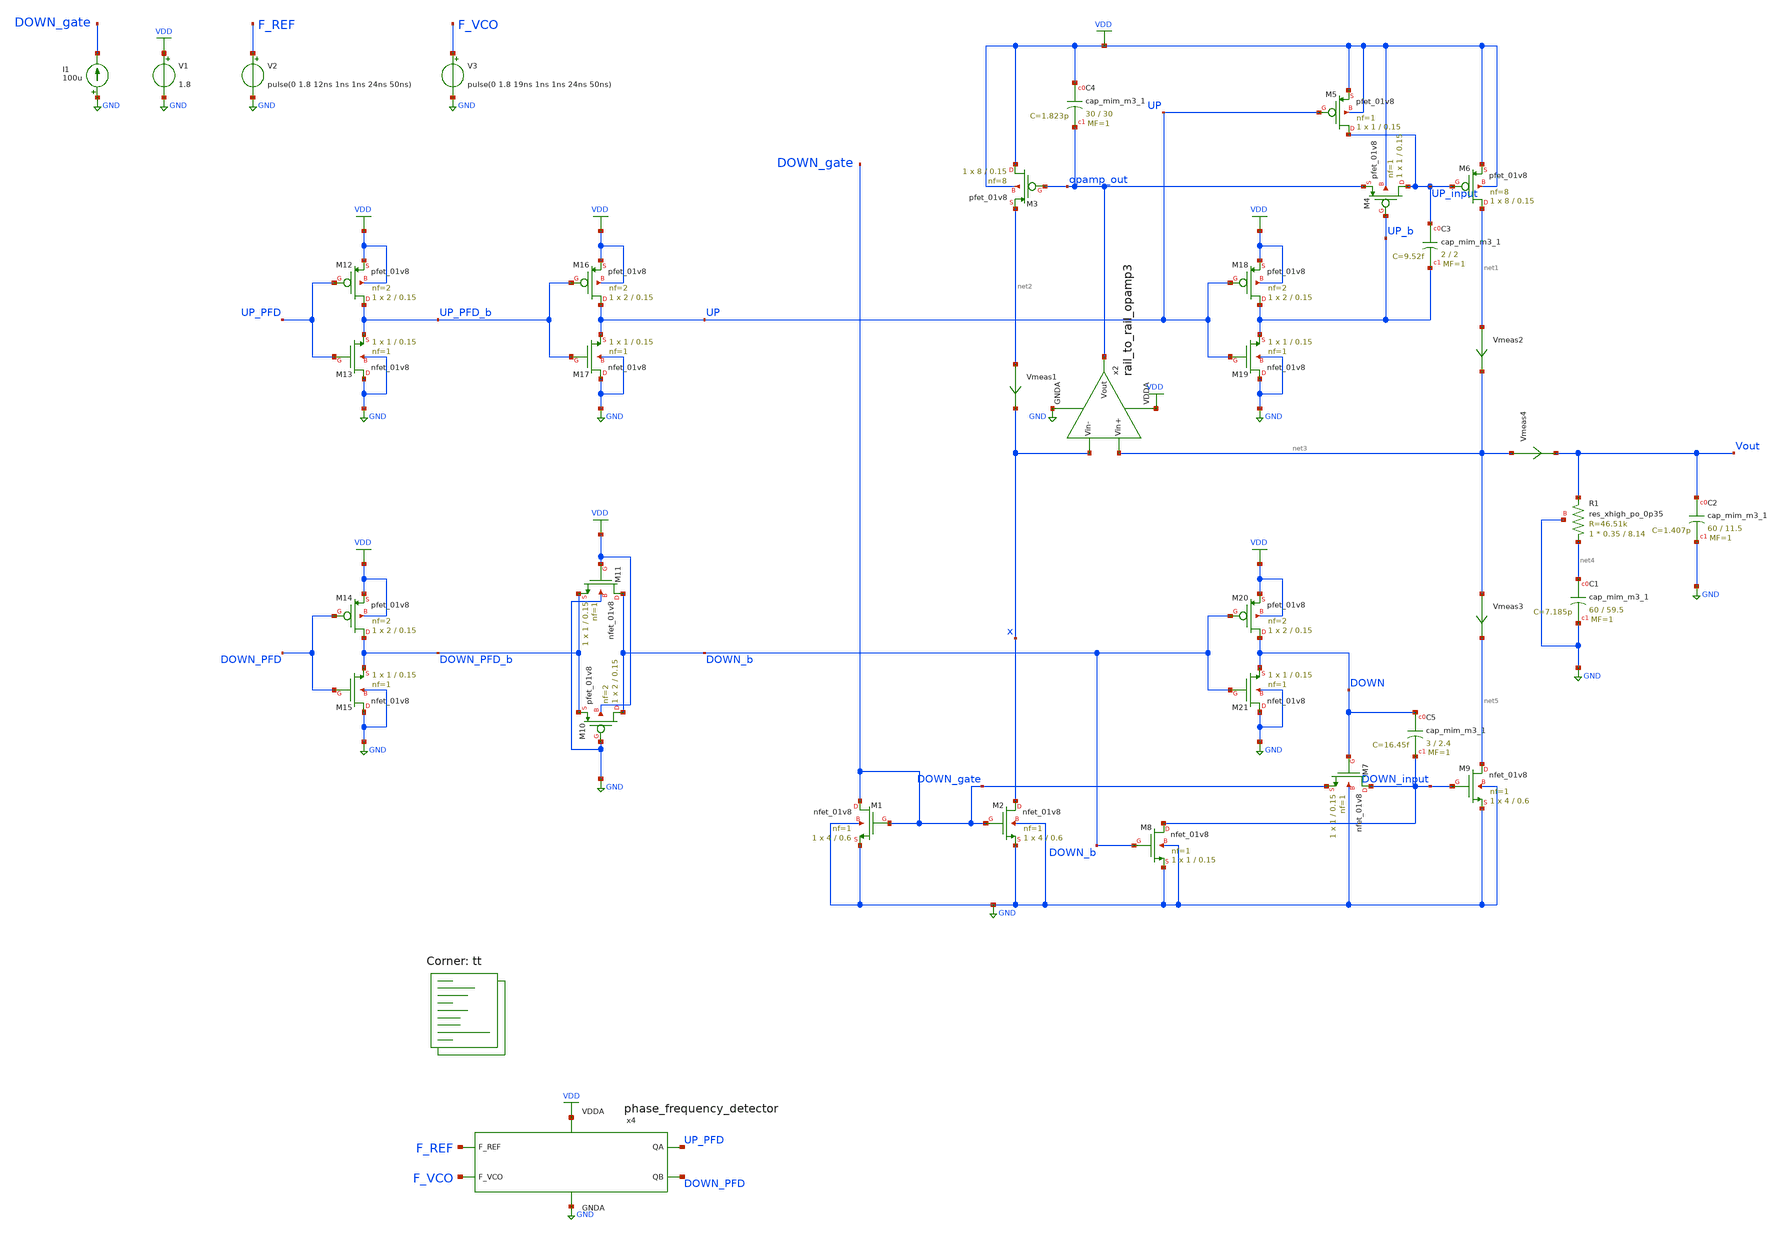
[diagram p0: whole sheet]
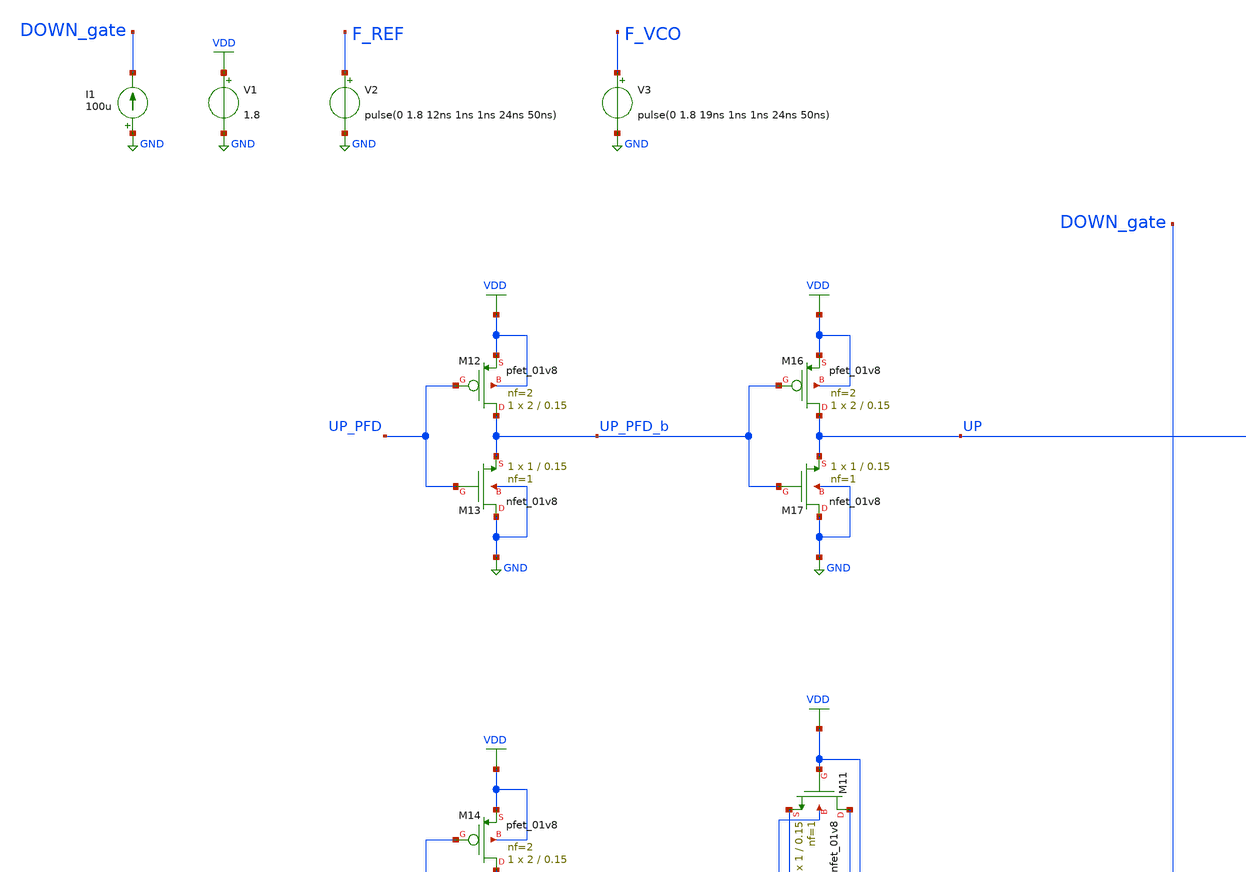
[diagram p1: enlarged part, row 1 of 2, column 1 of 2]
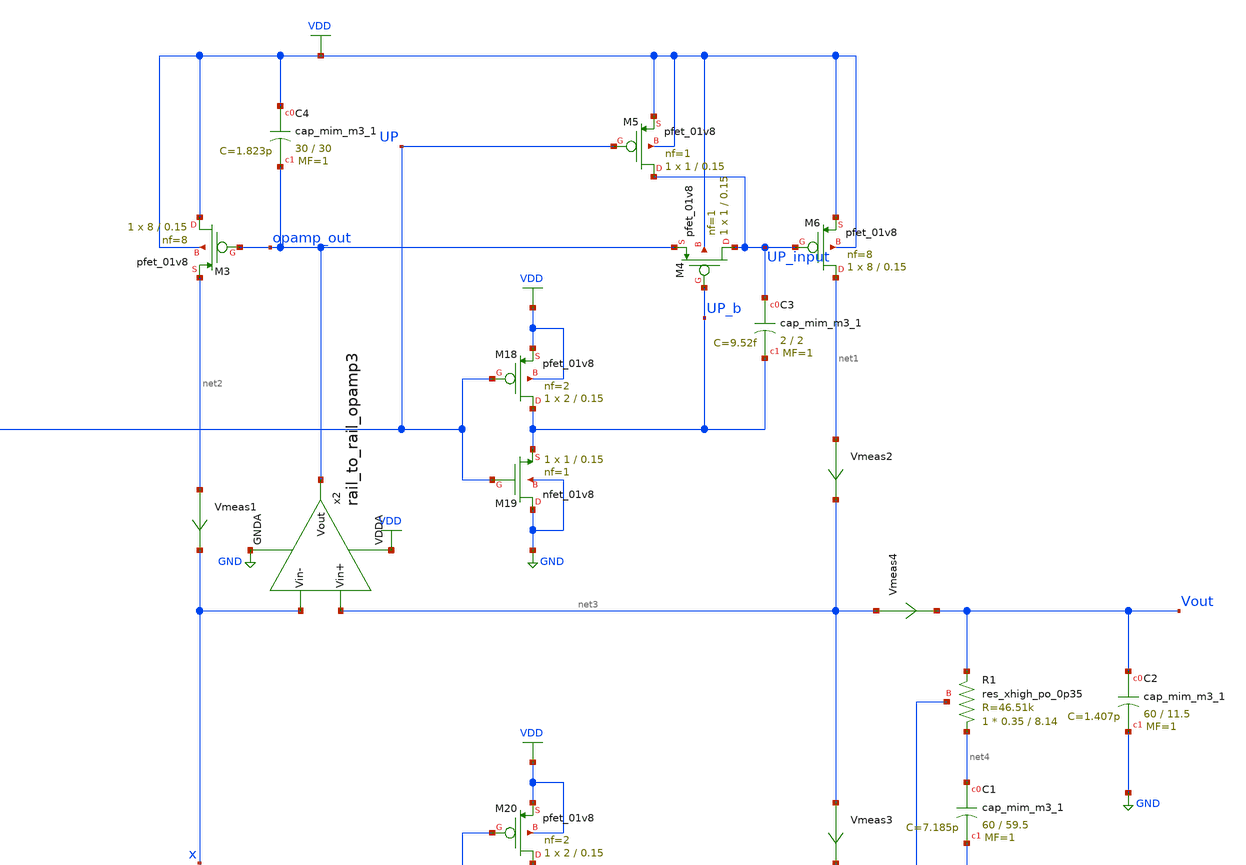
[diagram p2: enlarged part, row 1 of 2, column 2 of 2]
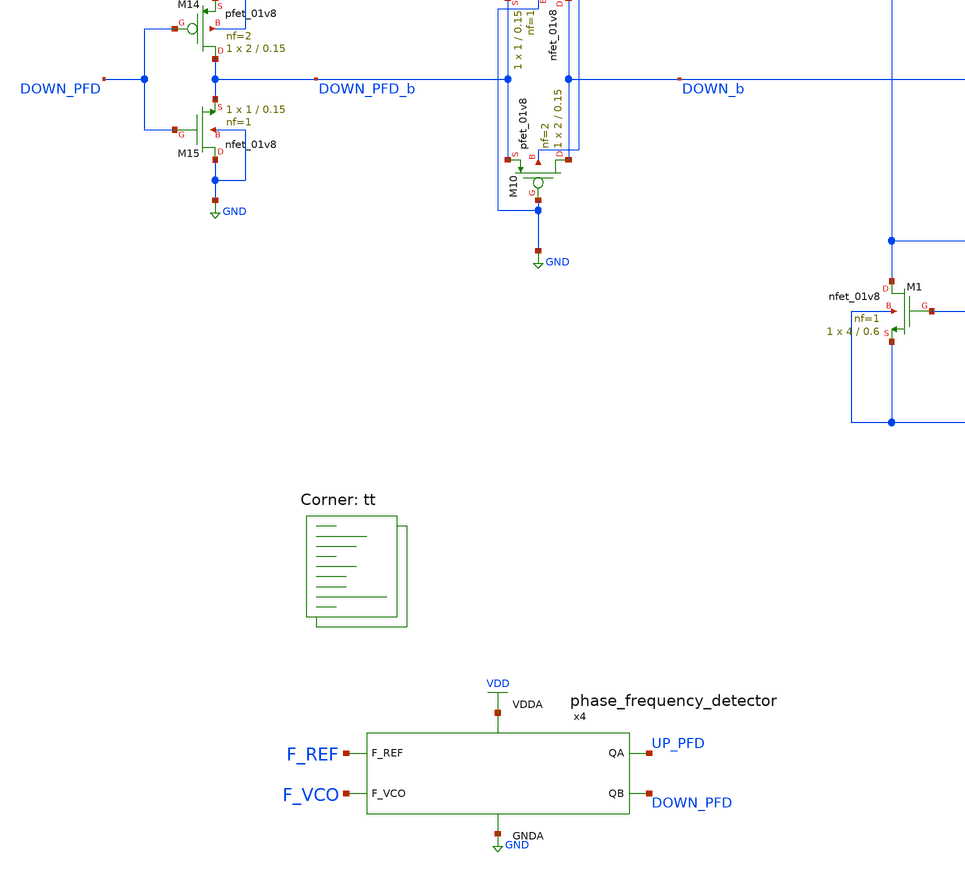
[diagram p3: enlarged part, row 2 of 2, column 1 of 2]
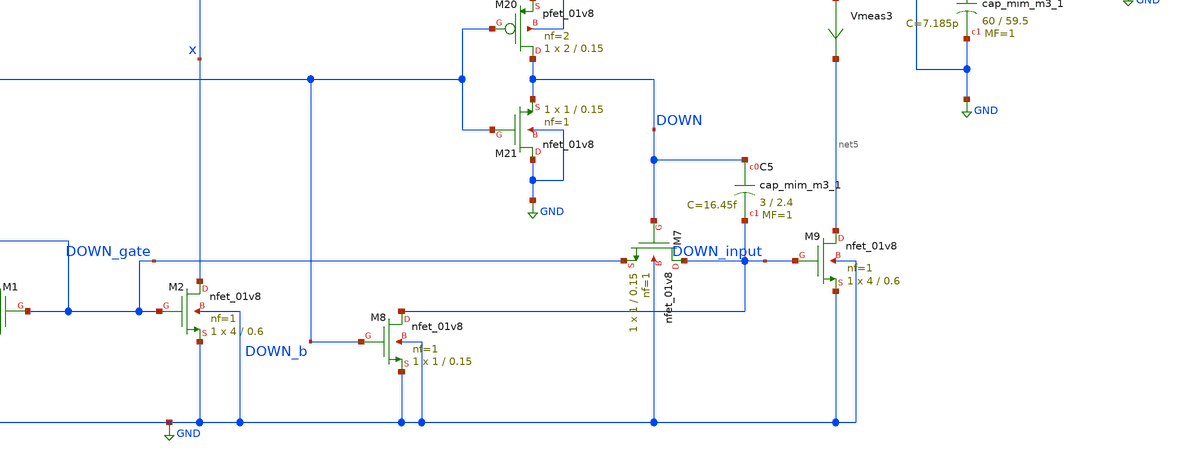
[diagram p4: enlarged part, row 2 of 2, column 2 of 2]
** sch_path: projects/pll/charge_pump/xschem_ngspice/pfd_charge_pump_7_2.sch
**.subckt pfd_charge_pump_7_2
V1 VDD GND 1.8
V2 F_REF GND pulse(0 1.8 12ns 1ns 1ns 24ns 50ns)
V3 F_VCO GND pulse(0 1.8 19ns 1ns 1ns 24ns 50ns)
x4 F_REF F_VCO VDD UP_PFD DOWN_PFD GND phase_frequency_detector
I1 GND DOWN_gate 100u
XM1 DOWN_gate DOWN_gate GND GND sky130_fd_pr__nfet_01v8 L=0.6 W=4 nf=1 ad='int((nf+1)/2) * W/nf * 0.29'
+ as='int((nf+2)/2) * W/nf * 0.29' pd='2*int((nf+1)/2) * (W/nf + 0.29)' ps='2*int((nf+2)/2) * (W/nf + 0.29)'
+ nrd='0.29 / W' nrs='0.29 / W' sa=0 sb=0 sd=0 mult=1 m=1
XM2 x DOWN_gate GND GND sky130_fd_pr__nfet_01v8 L=0.6 W=4 nf=1 ad='int((nf+1)/2) * W/nf * 0.29' as='int((nf+2)/2) * W/nf * 0.29'
+ pd='2*int((nf+1)/2) * (W/nf + 0.29)' ps='2*int((nf+2)/2) * (W/nf + 0.29)' nrd='0.29 / W' nrs='0.29 / W'
+ sa=0 sb=0 sd=0 mult=1 m=1
XM3 VDD opamp_out net2 VDD sky130_fd_pr__pfet_01v8 L=0.15 W=8 nf=8 ad='int((nf+1)/2) * W/nf * 0.29' as='int((nf+2)/2) * W/nf * 0.29'
+ pd='2*int((nf+1)/2) * (W/nf + 0.29)' ps='2*int((nf+2)/2) * (W/nf + 0.29)' nrd='0.29 / W' nrs='0.29 / W'
+ sa=0 sb=0 sd=0 mult=1 m=1
Vmeas1 net2 x 0
.save i(vmeas1)
XM4 UP_input UP_b opamp_out VDD sky130_fd_pr__pfet_01v8 L=0.15 W=1 nf=1 ad='int((nf+1)/2) * W/nf * 0.29'
+ as='int((nf+2)/2) * W/nf * 0.29' pd='2*int((nf+1)/2) * (W/nf + 0.29)' ps='2*int((nf+2)/2) * (W/nf + 0.29)'
+ nrd='0.29 / W' nrs='0.29 / W' sa=0 sb=0 sd=0 mult=1 m=1
XM5 UP_input UP VDD VDD sky130_fd_pr__pfet_01v8 L=0.15 W=1 nf=1 ad='int((nf+1)/2) * W/nf * 0.29' as='int((nf+2)/2) * W/nf * 0.29'
+ pd='2*int((nf+1)/2) * (W/nf + 0.29)' ps='2*int((nf+2)/2) * (W/nf + 0.29)' nrd='0.29 / W' nrs='0.29 / W'
+ sa=0 sb=0 sd=0 mult=1 m=1
XM6 net1 UP_input VDD VDD sky130_fd_pr__pfet_01v8 L=0.15 W=8 nf=8 ad='int((nf+1)/2) * W/nf * 0.29' as='int((nf+2)/2) * W/nf * 0.29'
+ pd='2*int((nf+1)/2) * (W/nf + 0.29)' ps='2*int((nf+2)/2) * (W/nf + 0.29)' nrd='0.29 / W' nrs='0.29 / W'
+ sa=0 sb=0 sd=0 mult=1 m=1
Vmeas2 net1 net3 0
.save i(vmeas2)
XM7 DOWN_input DOWN DOWN_gate GND sky130_fd_pr__nfet_01v8 L=0.15 W=1 nf=1 ad='int((nf+1)/2) * W/nf * 0.29'
+ as='int((nf+2)/2) * W/nf * 0.29' pd='2*int((nf+1)/2) * (W/nf + 0.29)' ps='2*int((nf+2)/2) * (W/nf + 0.29)'
+ nrd='0.29 / W' nrs='0.29 / W' sa=0 sb=0 sd=0 mult=1 m=1
XM8 DOWN_input DOWN_b GND GND sky130_fd_pr__nfet_01v8 L=0.15 W=1 nf=1 ad='int((nf+1)/2) * W/nf * 0.29'
+ as='int((nf+2)/2) * W/nf * 0.29' pd='2*int((nf+1)/2) * (W/nf + 0.29)' ps='2*int((nf+2)/2) * (W/nf + 0.29)'
+ nrd='0.29 / W' nrs='0.29 / W' sa=0 sb=0 sd=0 mult=1 m=1
Vmeas3 net3 net5 0
.save i(vmeas3)
XM9 net5 DOWN_input GND GND sky130_fd_pr__nfet_01v8 L=0.6 W=4 nf=1 ad='int((nf+1)/2) * W/nf * 0.29' as='int((nf+2)/2) * W/nf * 0.29'
+ pd='2*int((nf+1)/2) * (W/nf + 0.29)' ps='2*int((nf+2)/2) * (W/nf + 0.29)' nrd='0.29 / W' nrs='0.29 / W'
+ sa=0 sb=0 sd=0 mult=1 m=1
XC2 Vout GND sky130_fd_pr__cap_mim_m3_1 W=60 L=11.5 MF=1 m=1
XC1 net4 GND sky130_fd_pr__cap_mim_m3_1 W=60 L=59.5 MF=1 m=1
Vmeas4 net3 Vout 0
.save i(vmeas4)
x2 VDD net3 x opamp_out GND rail_to_rail_opamp3
XC4 VDD opamp_out sky130_fd_pr__cap_mim_m3_1 W=30 L=30 MF=1 m=1
XC3 UP_input UP_b sky130_fd_pr__cap_mim_m3_1 W=2 L=2 MF=1 m=1
XC5 DOWN DOWN_input sky130_fd_pr__cap_mim_m3_1 W=3 L=2.4 MF=1 m=1
XM10 DOWN_b GND DOWN_PFD_b VDD sky130_fd_pr__pfet_01v8 L=0.15 W=2 nf=2 ad='int((nf+1)/2) * W/nf * 0.29'
+ as='int((nf+2)/2) * W/nf * 0.29' pd='2*int((nf+1)/2) * (W/nf + 0.29)' ps='2*int((nf+2)/2) * (W/nf + 0.29)'
+ nrd='0.29 / W' nrs='0.29 / W' sa=0 sb=0 sd=0 mult=1 m=1
XM11 DOWN_b VDD DOWN_PFD_b GND sky130_fd_pr__nfet_01v8 L=0.15 W=1 nf=1 ad='int((nf+1)/2) * W/nf * 0.29'
+ as='int((nf+2)/2) * W/nf * 0.29' pd='2*int((nf+1)/2) * (W/nf + 0.29)' ps='2*int((nf+2)/2) * (W/nf + 0.29)'
+ nrd='0.29 / W' nrs='0.29 / W' sa=0 sb=0 sd=0 mult=1 m=1
XM12 UP_PFD_b UP_PFD VDD VDD sky130_fd_pr__pfet_01v8 L=0.15 W=2 nf=2 ad='int((nf+1)/2) * W/nf * 0.29'
+ as='int((nf+2)/2) * W/nf * 0.29' pd='2*int((nf+1)/2) * (W/nf + 0.29)' ps='2*int((nf+2)/2) * (W/nf + 0.29)'
+ nrd='0.29 / W' nrs='0.29 / W' sa=0 sb=0 sd=0 mult=1 m=1
XM13 GND UP_PFD UP_PFD_b GND sky130_fd_pr__nfet_01v8 L=0.15 W=1 nf=1 ad='int((nf+1)/2) * W/nf * 0.29'
+ as='int((nf+2)/2) * W/nf * 0.29' pd='2*int((nf+1)/2) * (W/nf + 0.29)' ps='2*int((nf+2)/2) * (W/nf + 0.29)'
+ nrd='0.29 / W' nrs='0.29 / W' sa=0 sb=0 sd=0 mult=1 m=1
XM14 DOWN_PFD_b DOWN_PFD VDD VDD sky130_fd_pr__pfet_01v8 L=0.15 W=2 nf=2 ad='int((nf+1)/2) * W/nf * 0.29'
+ as='int((nf+2)/2) * W/nf * 0.29' pd='2*int((nf+1)/2) * (W/nf + 0.29)' ps='2*int((nf+2)/2) * (W/nf + 0.29)'
+ nrd='0.29 / W' nrs='0.29 / W' sa=0 sb=0 sd=0 mult=1 m=1
XM15 GND DOWN_PFD DOWN_PFD_b GND sky130_fd_pr__nfet_01v8 L=0.15 W=1 nf=1 ad='int((nf+1)/2) * W/nf * 0.29'
+ as='int((nf+2)/2) * W/nf * 0.29' pd='2*int((nf+1)/2) * (W/nf + 0.29)' ps='2*int((nf+2)/2) * (W/nf + 0.29)'
+ nrd='0.29 / W' nrs='0.29 / W' sa=0 sb=0 sd=0 mult=1 m=1
XM16 UP UP_PFD_b VDD VDD sky130_fd_pr__pfet_01v8 L=0.15 W=2 nf=2 ad='int((nf+1)/2) * W/nf * 0.29' as='int((nf+2)/2) * W/nf * 0.29'
+ pd='2*int((nf+1)/2) * (W/nf + 0.29)' ps='2*int((nf+2)/2) * (W/nf + 0.29)' nrd='0.29 / W' nrs='0.29 / W'
+ sa=0 sb=0 sd=0 mult=1 m=1
XM17 GND UP_PFD_b UP GND sky130_fd_pr__nfet_01v8 L=0.15 W=1 nf=1 ad='int((nf+1)/2) * W/nf * 0.29' as='int((nf+2)/2) * W/nf * 0.29'
+ pd='2*int((nf+1)/2) * (W/nf + 0.29)' ps='2*int((nf+2)/2) * (W/nf + 0.29)' nrd='0.29 / W' nrs='0.29 / W'
+ sa=0 sb=0 sd=0 mult=1 m=1
XM18 UP_b UP VDD VDD sky130_fd_pr__pfet_01v8 L=0.15 W=2 nf=2 ad='int((nf+1)/2) * W/nf * 0.29' as='int((nf+2)/2) * W/nf * 0.29'
+ pd='2*int((nf+1)/2) * (W/nf + 0.29)' ps='2*int((nf+2)/2) * (W/nf + 0.29)' nrd='0.29 / W' nrs='0.29 / W'
+ sa=0 sb=0 sd=0 mult=1 m=1
XM19 GND UP UP_b GND sky130_fd_pr__nfet_01v8 L=0.15 W=1 nf=1 ad='int((nf+1)/2) * W/nf * 0.29' as='int((nf+2)/2) * W/nf * 0.29'
+ pd='2*int((nf+1)/2) * (W/nf + 0.29)' ps='2*int((nf+2)/2) * (W/nf + 0.29)' nrd='0.29 / W' nrs='0.29 / W'
+ sa=0 sb=0 sd=0 mult=1 m=1
XM20 DOWN DOWN_b VDD VDD sky130_fd_pr__pfet_01v8 L=0.15 W=2 nf=2 ad='int((nf+1)/2) * W/nf * 0.29' as='int((nf+2)/2) * W/nf * 0.29'
+ pd='2*int((nf+1)/2) * (W/nf + 0.29)' ps='2*int((nf+2)/2) * (W/nf + 0.29)' nrd='0.29 / W' nrs='0.29 / W'
+ sa=0 sb=0 sd=0 mult=1 m=1
XM21 GND DOWN_b DOWN GND sky130_fd_pr__nfet_01v8 L=0.15 W=1 nf=1 ad='int((nf+1)/2) * W/nf * 0.29' as='int((nf+2)/2) * W/nf * 0.29'
+ pd='2*int((nf+1)/2) * (W/nf + 0.29)' ps='2*int((nf+2)/2) * (W/nf + 0.29)' nrd='0.29 / W' nrs='0.29 / W'
+ sa=0 sb=0 sd=0 mult=1 m=1
XR1 net4 Vout GND sky130_fd_pr__res_xhigh_po_0p35 L=8.14 mult=1 m=1
**** begin user architecture code
.lib $::SKYWATER_MODELS/sky130.lib.spice tt



.include /foss/pdks/sky130A/libs.ref/sky130_fd_sc_hd/spice/sky130_fd_sc_hd.spice

.option method=gear
.option wnflag=1

.ic v(vout) = 0.9
* .ic v(vout) = 1.8

.control
  save v(up_pfd) v(down_pfd) v(up_pfd_b) v(down_pfd_b) v(up) v(up_b) v(down) v(down_b) v(x) v(vout)
+ v(up_input) v(down_input)
  * save all

  tran 50ps 0.5us
  remzerovec
  write pfd_charge_pump_7_2.raw
  set appendwrite

.endc



**** end user architecture code
**.ends
.GLOBAL GND
.GLOBAL VDD
.end
